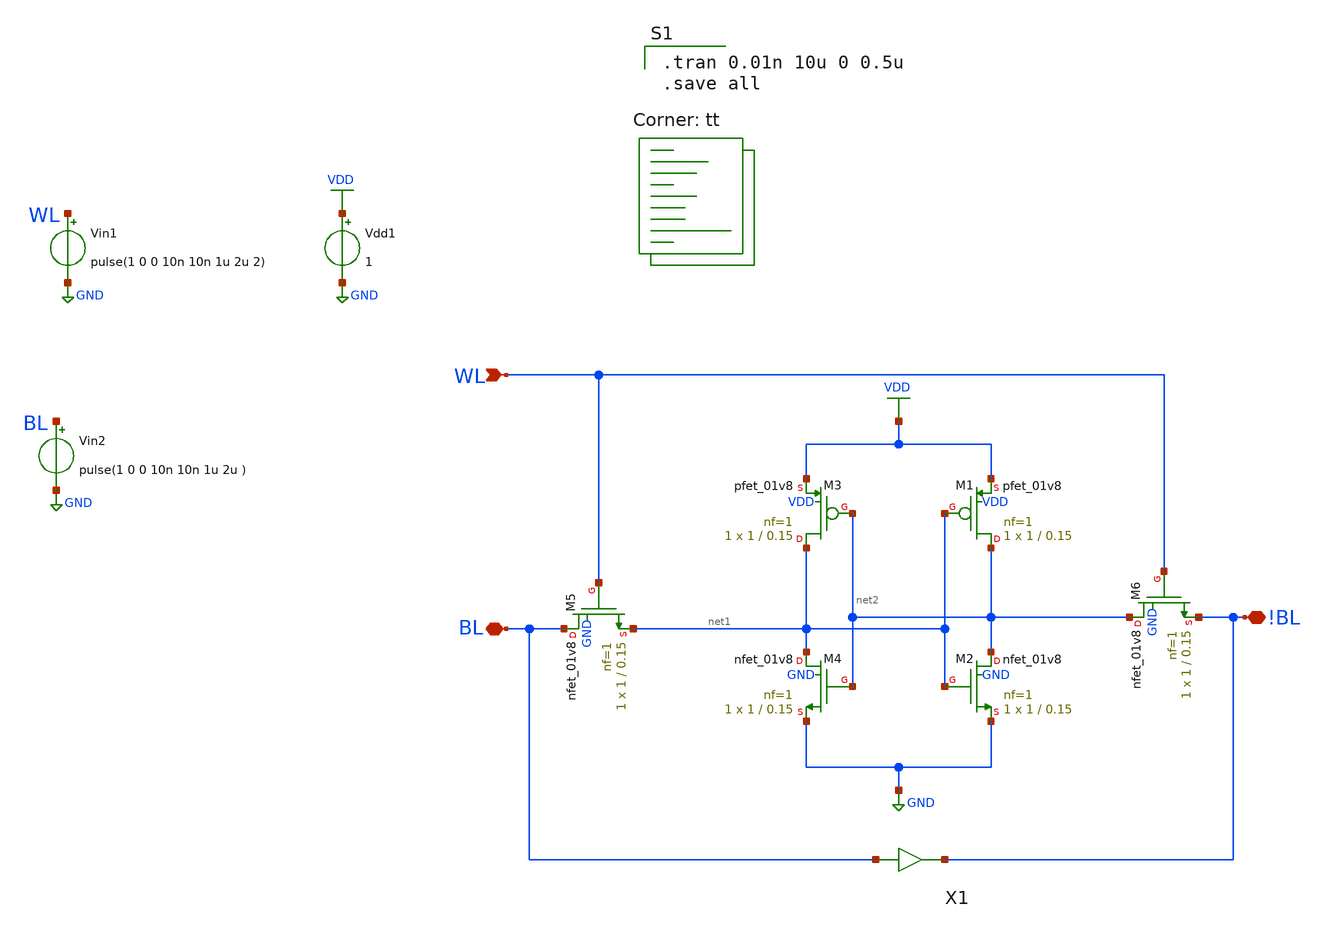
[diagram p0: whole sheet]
** sch_path: gates/Memory/1 bit 6-T SRAMsim.sch
**.subckt 1 bit 6-T SRAMsim WL BL !BL
*.ipin WL
*.iopin BL
*.iopin !BL
XM1 net2 net1 VDD VDD sky130_fd_pr__pfet_01v8 L=0.15 W=1 nf=1 ad='int((nf+1)/2) * W/nf * 0.29' as='int((nf+2)/2) * W/nf * 0.29'
+ pd='2*int((nf+1)/2) * (W/nf + 0.29)' ps='2*int((nf+2)/2) * (W/nf + 0.29)' nrd='0.29 / W' nrs='0.29 / W'
+ sa=0 sb=0 sd=0 mult=1 m=1
XM2 net2 net1 GND GND sky130_fd_pr__nfet_01v8 L=0.15 W=1 nf=1 ad='int((nf+1)/2) * W/nf * 0.29' as='int((nf+2)/2) * W/nf * 0.29'
+ pd='2*int((nf+1)/2) * (W/nf + 0.29)' ps='2*int((nf+2)/2) * (W/nf + 0.29)' nrd='0.29 / W' nrs='0.29 / W'
+ sa=0 sb=0 sd=0 mult=1 m=1
XM3 net1 net2 VDD VDD sky130_fd_pr__pfet_01v8 L=0.15 W=1 nf=1 ad='int((nf+1)/2) * W/nf * 0.29' as='int((nf+2)/2) * W/nf * 0.29'
+ pd='2*int((nf+1)/2) * (W/nf + 0.29)' ps='2*int((nf+2)/2) * (W/nf + 0.29)' nrd='0.29 / W' nrs='0.29 / W'
+ sa=0 sb=0 sd=0 mult=1 m=1
XM4 net1 net2 GND GND sky130_fd_pr__nfet_01v8 L=0.15 W=1 nf=1 ad='int((nf+1)/2) * W/nf * 0.29' as='int((nf+2)/2) * W/nf * 0.29'
+ pd='2*int((nf+1)/2) * (W/nf + 0.29)' ps='2*int((nf+2)/2) * (W/nf + 0.29)' nrd='0.29 / W' nrs='0.29 / W'
+ sa=0 sb=0 sd=0 mult=1 m=1
XM5 BL WL net1 GND sky130_fd_pr__nfet_01v8 L=0.15 W=1 nf=1 ad='int((nf+1)/2) * W/nf * 0.29' as='int((nf+2)/2) * W/nf * 0.29'
+ pd='2*int((nf+1)/2) * (W/nf + 0.29)' ps='2*int((nf+2)/2) * (W/nf + 0.29)' nrd='0.29 / W' nrs='0.29 / W'
+ sa=0 sb=0 sd=0 mult=1 m=1
XM6 net2 WL !BL GND sky130_fd_pr__nfet_01v8 L=0.15 W=1 nf=1 ad='int((nf+1)/2) * W/nf * 0.29' as='int((nf+2)/2) * W/nf * 0.29'
+ pd='2*int((nf+1)/2) * (W/nf + 0.29)' ps='2*int((nf+2)/2) * (W/nf + 0.29)' nrd='0.29 / W' nrs='0.29 / W'
+ sa=0 sb=0 sd=0 mult=1 m=1
Vdd1 VDD GND 1
Vin1 WL GND pulse(1 0 0 10n 10n 1u 2u 2)
Vin2 BL GND pulse(1 0 0 10n 10n 1u 2u )
X1 BL !BL inv_vtc
**** begin user architecture code

.tran 0.01n 10u 0 0.5u
.save all

.lib $::SKYWATER_MODELS/sky130.lib.spice tt
**** end user architecture code
**.ends

* expanding   symbol:  /home/apn/test_xschem_sky130/inv_vtc.sym # of pins=2
** sym_path: gates/Memory/inv_vtc.sym
** sch_path: gates/Memory/inv_vtc.sch
.subckt inv_vtc A Y
*.ipin A
*.opin Y
XM1 Y A VDD VDD sky130_fd_pr__pfet_01v8 L=0.15 W=2 nf=1 ad='int((nf+1)/2) * W/nf * 0.29' as='int((nf+2)/2) * W/nf * 0.29'
+ pd='2*int((nf+1)/2) * (W/nf + 0.29)' ps='2*int((nf+2)/2) * (W/nf + 0.29)' nrd='0.29 / W' nrs='0.29 / W'
+ sa=0 sb=0 sd=0 mult=1 m=1
XM2 Y A GND GND sky130_fd_pr__nfet_01v8 L=0.15 W=1 nf=1 ad='int((nf+1)/2) * W/nf * 0.29' as='int((nf+2)/2) * W/nf * 0.29'
+ pd='2*int((nf+1)/2) * (W/nf + 0.29)' ps='2*int((nf+2)/2) * (W/nf + 0.29)' nrd='0.29 / W' nrs='0.29 / W'
+ sa=0 sb=0 sd=0 mult=1 m=1
.ends

.GLOBAL GND
.GLOBAL VDD
.end
